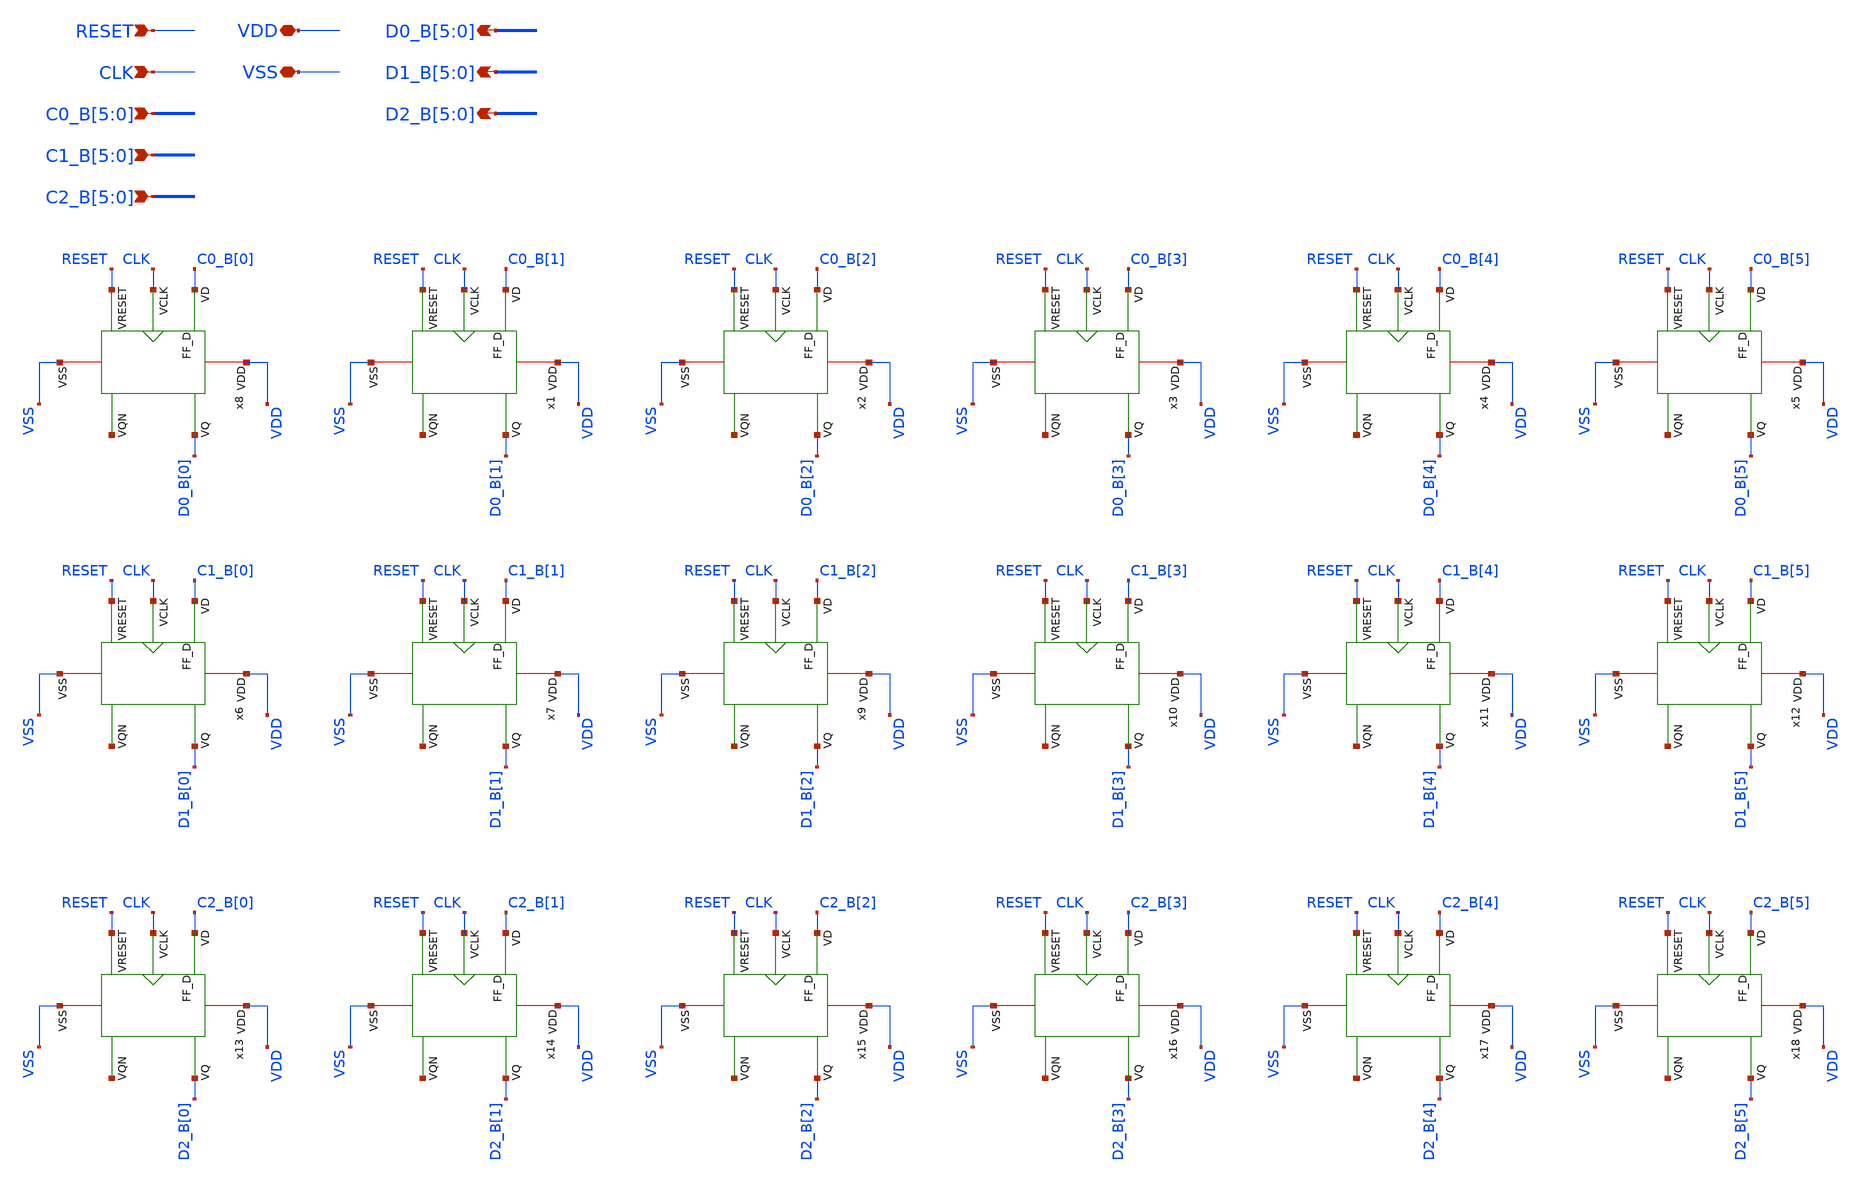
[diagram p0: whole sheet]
** sch_path: ADC8711-main/schematic/xschem/Counters_regs_6bits.sch
**.subckt Counters_regs_6bits VDD VSS RESET C0_B[5],C0_B[4],C0_B[3],C0_B[2],C0_B[1],C0_B[0]
*+ C1_B[5],C1_B[4],C1_B[3],C1_B[2],C1_B[1],C1_B[0] C2_B[5],C2_B[4],C2_B[3],C2_B[2],C2_B[1],C2_B[0] D0_B[5],D0_B[4],D0_B[3],D0_B[2],D0_B[1],D0_B[0]
*+ D1_B[5],D1_B[4],D1_B[3],D1_B[2],D1_B[1],D1_B[0] D2_B[5],D2_B[4],D2_B[3],D2_B[2],D2_B[1],D2_B[0] CLK
*.iopin VDD
*.iopin VSS
*.ipin RESET
*.ipin C0_B[5],C0_B[4],C0_B[3],C0_B[2],C0_B[1],C0_B[0]
*.ipin C1_B[5],C1_B[4],C1_B[3],C1_B[2],C1_B[1],C1_B[0]
*.ipin C2_B[5],C2_B[4],C2_B[3],C2_B[2],C2_B[1],C2_B[0]
*.opin D0_B[5],D0_B[4],D0_B[3],D0_B[2],D0_B[1],D0_B[0]
*.opin D1_B[5],D1_B[4],D1_B[3],D1_B[2],D1_B[1],D1_B[0]
*.opin D2_B[5],D2_B[4],D2_B[3],D2_B[2],D2_B[1],D2_B[0]
*.ipin CLK
x8 VDD CLK RESET VSS D0_B[0] net1 C0_B[0] FF_D
x1 VDD CLK RESET VSS D0_B[1] net2 C0_B[1] FF_D
x2 VDD CLK RESET VSS D0_B[2] net3 C0_B[2] FF_D
x3 VDD CLK RESET VSS D0_B[3] net4 C0_B[3] FF_D
x4 VDD CLK RESET VSS D0_B[4] net5 C0_B[4] FF_D
x5 VDD CLK RESET VSS D0_B[5] net6 C0_B[5] FF_D
x6 VDD CLK RESET VSS D1_B[0] net7 C1_B[0] FF_D
x7 VDD CLK RESET VSS D1_B[1] net8 C1_B[1] FF_D
x9 VDD CLK RESET VSS D1_B[2] net9 C1_B[2] FF_D
x10 VDD CLK RESET VSS D1_B[3] net10 C1_B[3] FF_D
x11 VDD CLK RESET VSS D1_B[4] net11 C1_B[4] FF_D
x12 VDD CLK RESET VSS D1_B[5] net12 C1_B[5] FF_D
x13 VDD CLK RESET VSS D2_B[0] net13 C2_B[0] FF_D
x14 VDD CLK RESET VSS D2_B[1] net14 C2_B[1] FF_D
x15 VDD CLK RESET VSS D2_B[2] net15 C2_B[2] FF_D
x16 VDD CLK RESET VSS D2_B[3] net16 C2_B[3] FF_D
x17 VDD CLK RESET VSS D2_B[4] net17 C2_B[4] FF_D
x18 VDD CLK RESET VSS D2_B[5] net18 C2_B[5] FF_D
**.ends
.end
